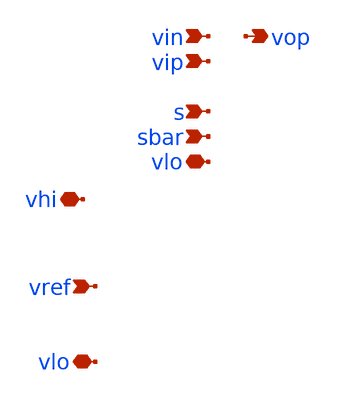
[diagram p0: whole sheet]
** sch_path: xschem/i_type_ota_gb_rp_gp_PEX.sch
**.subckt i_type_ota_gb_rp_gp_PEX vip vin vop vhi vlo vref s sbar vlo
*.ipin vip
*.ipin vin
*.opin vop
*.iopin vhi
*.iopin vlo
*.ipin vref
*.ipin s
*.ipin sbar
*.iopin vlo
**** begin user architecture code

* NGSPICE file created from cmota_1_flat.ext - technology: sky130A
* NGSPICE file created from cmota_gb_rp_gp.ext - technology: sky130A
.subckt imirror2 OUT a_5468_1540# a_4094_1540# a_4493_207# VLO VHI a_5868_1637# IN  a_4036_1637#
X0 VHI a_4493_207# a_4493_207# VHI.t5 sky130_fd_pr__pfet_01v8 ad=2.9e+12p pd=2.058e+07u as=2.9e+12p
+ ps=2.058e+07u w=1e+07u l=2e+06u
X1 a_4493_207# VLO.t6 VLO.t8 VLO.t7 sky130_fd_pr__nfet_01v8 ad=1.45e+12p pd=1.058e+07u as=0p ps=0u
+ w=5e+06u l=2e+06u
X2 VLO.t5 VLO.t3 OUT VLO.t4 sky130_fd_pr__nfet_01v8 ad=0p pd=0u as=1.45e+12p ps=1.058e+07u w=5e+06u
+ l=2e+06u
X3 a_5868_1637# a_5468_1540# OUT VHI.t0 sky130_fd_pr__pfet_01v8 ad=2.9e+12p pd=2.058e+07u
+ as=2.9e+12p ps=2.058e+07u w=1e+07u l=2e+06u
X4 OUT OUT.t0 VLO VLO.t0 sky130_fd_pr__nfet_01v8 ad=0p pd=0u as=4.35e+12p ps=3.174e+07u w=5e+06u
+ l=2e+06u
X5 VLO IN.t0 a_4493_207# VLO.t9 sky130_fd_pr__nfet_01v8 ad=0p pd=0u as=0p ps=0u w=5e+06u l=2e+06u
X6 a_4493_207# a_4094_1540# a_4036_1637# VHI.t1 sky130_fd_pr__pfet_01v8 ad=0p pd=0u as=2.9e+12p
+ ps=2.058e+07u w=1e+07u l=2e+06u
X7 OUT a_4493_207# VHI VHI.t2 sky130_fd_pr__pfet_01v8 ad=0p pd=0u as=0p ps=0u w=1e+07u l=2e+06u
R0 VHI.t2 VHI.t0 178.465
R1 VHI.t5 VHI.t1 178.465
R2 VHI.t0 VHI.n1 133.656
R3 VHI.t1 VHI.n3 133.656
R4 VHI.n6 VHI.t2 89.232
R5 VHI.n6 VHI.t5 89.232
R6 VHI.n9 VHI.n8 3.388
R7 VHI VHI.n9 1.702
R8 VHI.n5 VHI.n4 0.002
R9 VHI.n6 VHI.n5 0.002
R10 VHI.n8 VHI.n7 0.002
R11 VHI.n7 VHI.n6 0.002
R12 VHI.n3 VHI.n2 0.002
R13 VHI.n1 VHI.n0 0.002
R14 VLO.n4 VLO.t4 1062.83
R15 VLO.n7 VLO.t7 1062.83
R16 VLO.n15 VLO.t0 709.577
R17 VLO.n15 VLO.t9 709.577
R18 VLO.n13 VLO.n11 344.847
R19 VLO.n13 VLO.n12 344.847
R20 VLO.n6 VLO.n5 264.873
R21 VLO.n9 VLO.n8 264.496
R22 VLO.n21 VLO.n19 202.541
R23 VLO.n2 VLO.n0 202.541
R24 VLO.t6 VLO.n20 153.089
R25 VLO.n21 VLO.t6 153.089
R26 VLO.n2 VLO.t3 153.089
R27 VLO.t3 VLO.n1 153.089
R28 VLO.n22 VLO.n21 32.935
R29 VLO.n3 VLO.n2 32.935
R30 VLO.n24 VLO.n9 10.039
R31 VLO.n24 VLO.n6 10.037
R32 VLO.n24 VLO.n18 8.178
R33 VLO.n24 VLO.n23 8.178
R34 VLO.n23 VLO.n22 8.01
R35 VLO.n6 VLO.n3 6.032
R36 VLO.n24 VLO.n17 3.765
R37 VLO.n19 VLO.t8 3.48
R38 VLO.n0 VLO.t5 3.48
R39 VLO VLO.n24 1.562
R40 VLO.n17 VLO.n10 1.127
R41 VLO.n17 VLO.n16 0.014
R42 VLO.n16 VLO.n15 0.014
R43 VLO.n8 VLO.n7 0.012
R44 VLO.n5 VLO.n4 0.012
R45 VLO.n14 VLO.n13 0.007
R46 VLO.n15 VLO.n14 0.007
R47 OUT OUT.t0 68.216
R48 IN IN.t0 67.356
C0 a_4036_1637# VHI 0.68fF
C1 a_4493_207# VHI 3.25fF
C2 a_5468_1540# a_5868_1637# 0.15fF
C3 a_4094_1540# a_5868_1637# 0.01fF
C4 a_4493_207# a_4036_1637# 0.63fF
C5 IN OUT 0.22fF
C6 a_5468_1540# OUT 0.53fF
C7 a_4094_1540# OUT 0.10fF
C8 IN VHI 0.19fF
C9 a_5468_1540# VHI 0.99fF
C10 a_4036_1637# IN 0.03fF
C11 a_4094_1540# VHI 0.99fF
C12 a_4493_207# IN 0.46fF
C13 a_5468_1540# a_4036_1637# 0.01fF
C14 a_4493_207# a_5468_1540# 0.22fF
C15 a_4094_1540# a_4036_1637# 0.15fF
C16 a_4094_1540# a_4493_207# 0.44fF
C17 a_5868_1637# OUT 0.47fF
C18 a_5868_1637# VHI 0.45fF
C19 a_4493_207# a_5868_1637# 0.22fF
C20 a_4094_1540# IN 0.17fF
C21 a_4094_1540# a_5468_1540# 0.00fF
C22 VHI OUT 1.31fF
C23 a_4036_1637# OUT 0.03fF
C24 a_4493_207# OUT 0.88fF
C25 OUT VLO 5.14fF
C26 VHI VLO 19.08fF
C27 IN VLO 2.36fF
C28 a_5868_1637# VLO 0.34fF
C29 a_4036_1637# VLO 0.34fF
C30 a_5468_1540# VLO 0.34fF
C31 a_4493_207# VLO 1.55fF
C32 a_4094_1540# VLO 0.34fF
C33 OUT.t0 VLO 1.25fF
C34 VHI.n0 VLO 0.25fF $ **FLOATING
C35 VHI.n1 VLO 2.09fF $ **FLOATING
C36 VHI.t0 VLO 3.29fF
C37 VHI.t2 VLO 2.82fF
C38 VHI.n2 VLO 0.25fF $ **FLOATING
C39 VHI.n3 VLO 2.09fF $ **FLOATING
C40 VHI.t1 VLO 3.29fF
C41 VHI.t5 VLO 2.82fF
C42 VHI.n4 VLO 0.25fF $ **FLOATING
C43 VHI.n5 VLO 0.25fF $ **FLOATING
C44 VHI.n6 VLO 1.88fF $ **FLOATING
C45 VHI.n7 VLO 0.25fF $ **FLOATING
C46 VHI.n8 VLO 0.13fF $ **FLOATING
C47 VHI.n9 VLO 2.08fF $ **FLOATING
.ends

.subckt gated_iref_fix imirror2_0/a_5468_1540# imirror2_0/a_4094_1540# SBAR a_1444_106#
+  imirror2_0/OUT imirror2_0/a_5868_1637# VSUB imirror2_0/VHI imirror2_0/a_4493_207#  imirror2_0/a_4036_1637#
+ a_1712_150# S imirror2_0/IN
Ximirror2_0 imirror2_0/OUT imirror2_0/a_5468_1540# imirror2_0/a_4094_1540# imirror2_0/a_4493_207#
+  VSUB imirror2_0/VHI imirror2_0/a_5868_1637# imirror2_0/IN imirror2_0/a_4036_1637#  imirror2
X0 imirror2_0/OUT a_1444_106# VSUB sky130_fd_pr__res_xhigh_po w=350000u l=1.49e+06u
X1 VSUB SBAR a_1712_150# VSUB sky130_fd_pr__nfet_01v8 ad=5.95e+12p pd=4.302e+07u as=1.65e+12p
+ ps=1.132e+07u w=2.5e+06u l=150000u
X2 VSUB a_1712_150# sky130_fd_pr__cap_mim_m3_1 l=6.2e+06u w=2.76e+07u
X3 a_1712_150# VSUB sky130_fd_pr__cap_mim_m3_2 l=6.2e+06u w=2.76e+07u
X4 a_1712_150# S a_1444_106# VSUB sky130_fd_pr__nfet_01v8 ad=0p pd=0u as=1.6e+12p ps=1.128e+07u
+ w=2.5e+06u l=150000u
X5 VSUB VSUB a_1444_106# VSUB sky130_fd_pr__nfet_01v8 ad=0p pd=0u as=0p ps=0u w=2.5e+06u l=150000u
X6 a_1712_150# SBAR VSUB VSUB sky130_fd_pr__nfet_01v8 ad=0p pd=0u as=0p ps=0u w=2.5e+06u l=150000u
X7 a_1444_106# S a_1712_150# VSUB sky130_fd_pr__nfet_01v8 ad=0p pd=0u as=0p ps=0u w=2.5e+06u
+ l=150000u
C0 a_1712_150# imirror2_0/a_5868_1637# 0.33fF
C1 imirror2_0/OUT S 0.13fF
C2 imirror2_0/VHI imirror2_0/OUT 0.03fF
C3 imirror2_0/OUT imirror2_0/a_4493_207# 0.00fF
C4 a_1444_106# a_1712_150# 0.93fF
C5 SBAR a_1444_106# 0.07fF
C6 S a_1712_150# 0.27fF
C7 S SBAR 0.71fF
C8 imirror2_0/OUT a_1712_150# 1.57fF
C9 imirror2_0/VHI a_1712_150# 0.88fF
C10 imirror2_0/OUT SBAR 0.14fF
C11 a_1444_106# imirror2_0/IN 0.00fF
C12 S imirror2_0/IN 0.01fF
C13 a_1712_150# imirror2_0/a_4493_207# 0.29fF
C14 imirror2_0/OUT imirror2_0/IN 0.07fF
C15 imirror2_0/VHI imirror2_0/IN 0.00fF
C16 imirror2_0/OUT imirror2_0/a_5468_1540# 0.00fF
C17 SBAR a_1712_150# 0.25fF
C18 imirror2_0/a_4493_207# imirror2_0/IN 0.12fF
C19 a_1712_150# imirror2_0/IN 0.12fF
C20 SBAR imirror2_0/IN 0.01fF
C21 a_1712_150# imirror2_0/a_5468_1540# 0.33fF
C22 imirror2_0/OUT imirror2_0/a_5868_1637# 0.00fF
C23 S a_1444_106# 0.03fF
C24 imirror2_0/OUT a_1444_106# 0.33fF
C25 a_1712_150# VSUB 39.40fF
C26 a_1444_106# VSUB 1.29fF
C27 SBAR VSUB 0.76fF
C28 S VSUB 0.77fF
C29 imirror2_0/OUT VSUB 6.83fF
C30 imirror2_0/VHI VSUB 19.56fF
C31 imirror2_0/IN VSUB 4.59fF
C32 imirror2_0/a_5868_1637# VSUB 0.44fF
C33 imirror2_0/a_4036_1637# VSUB 0.34fF
C34 imirror2_0/a_5468_1540# VSUB 0.49fF
C35 imirror2_0/a_4493_207# VSUB 1.64fF
C36 imirror2_0/a_4094_1540# VSUB 0.34fF
C37 imirror2_0/OUT.t0 VSUB 1.25fF $ **FLOATING
C38 imirror2_0/VHI.n0 VSUB 0.25fF $ **FLOATING
C39 imirror2_0/VHI.n1 VSUB 2.09fF $ **FLOATING
C40 imirror2_0/VHI.t0 VSUB 3.29fF $ **FLOATING
C41 imirror2_0/VHI.t2 VSUB 2.82fF $ **FLOATING
C42 imirror2_0/VHI.n2 VSUB 0.25fF $ **FLOATING
C43 imirror2_0/VHI.n3 VSUB 2.09fF $ **FLOATING
C44 imirror2_0/VHI.t1 VSUB 3.29fF $ **FLOATING
C45 imirror2_0/VHI.t5 VSUB 2.82fF $ **FLOATING
C46 imirror2_0/VHI.n4 VSUB 0.25fF $ **FLOATING
C47 imirror2_0/VHI.n5 VSUB 0.25fF $ **FLOATING
C48 imirror2_0/VHI.n6 VSUB 1.88fF $ **FLOATING
C49 imirror2_0/VHI.n7 VSUB 0.25fF $ **FLOATING
C50 imirror2_0/VHI.n8 VSUB 0.13fF $ **FLOATING
C51 imirror2_0/VHI.n9 VSUB 2.08fF $ **FLOATING
.ends

.subckt sky130_fd_pr__res_high_po_0p69_G8QCSG a_48_n518# a_n186_n518# a_n316_n648#
X0 a_n186_n518# a_48_n518# a_n316_n648# sky130_fd_pr__res_high_po w=690000u l=5.83e+06u
C0 a_n186_n518# a_48_n518# 0.18fF
C1 a_48_n518# a_n316_n648# 0.52fF
C2 a_n186_n518# a_n316_n648# 0.52fF
.ends

.subckt cmota_gb_rp VREF COM VIP VIN DP li_5300_n960# VLO a_2217_285# DN VOP VMN VHI  a_2925_285#
Xsky130_fd_pr__res_high_po_0p69_G8QCSG_0 li_5300_n960# VMN VLO sky130_fd_pr__res_high_po_0p69_G8QCSG
X0 VHI DN VMN VHI sky130_fd_pr__pfet_01v8 ad=4.93e+13p pd=3.4986e+08u as=1.16e+13p ps=8.232e+07u
+ w=1e+07u l=300000u
X1 VHI DN DN VHI sky130_fd_pr__pfet_01v8 ad=0p pd=0u as=8.7e+12p ps=6.174e+07u w=1e+07u l=300000u
X2 VHI DP VOP VHI sky130_fd_pr__pfet_01v8 ad=0p pd=0u as=1.16e+13p ps=8.232e+07u w=1e+07u l=300000u
X3 DN VIN COM VLO sky130_fd_pr__nfet_01v8_lvt ad=3.3e+12p pd=2.264e+07u as=1.3225e+13p ps=9.21e+07u
+ w=2.5e+06u l=150000u
X4 COM VIN DN VLO sky130_fd_pr__nfet_01v8_lvt ad=0p pd=0u as=0p ps=0u w=2.5e+06u l=150000u
X5 DP VIP COM VLO sky130_fd_pr__nfet_01v8_lvt ad=3.3e+12p pd=2.264e+07u as=0p ps=0u w=2.5e+06u
+ l=150000u
X6 VMN DN VHI VHI sky130_fd_pr__pfet_01v8 ad=0p pd=0u as=0p ps=0u w=1e+07u l=300000u
X7 VMN DN VHI VHI sky130_fd_pr__pfet_01v8 ad=0p pd=0u as=0p ps=0u w=1e+07u l=300000u
X8 VHI VHI VOP VHI sky130_fd_pr__pfet_01v8 ad=0p pd=0u as=0p ps=0u w=1e+07u l=300000u
X9 a_2925_285# DN VHI VHI sky130_fd_pr__pfet_01v8 ad=2.9e+12p pd=2.058e+07u as=0p ps=0u w=1e+07u
+ l=300000u
X10 DP VIP COM VLO sky130_fd_pr__nfet_01v8_lvt ad=0p pd=0u as=0p ps=0u w=2.5e+06u l=150000u
X11 li_5300_n960# VOP sky130_fd_pr__cap_mim_m3_2 l=1.32e+07u w=3.7e+06u
X12 VOP DP VHI VHI sky130_fd_pr__pfet_01v8 ad=0p pd=0u as=0p ps=0u w=1e+07u l=300000u
X13 VOP DP VHI VHI sky130_fd_pr__pfet_01v8 ad=0p pd=0u as=0p ps=0u w=1e+07u l=300000u
X14 VOP DP VHI VHI sky130_fd_pr__pfet_01v8 ad=0p pd=0u as=0p ps=0u w=1e+07u l=300000u
X15 COM VLO VLO VLO sky130_fd_pr__nfet_01v8_lvt ad=0p pd=0u as=3.8e+13p ps=2.69525e+08u w=2.5e+06u
+ l=150000u
X16 VLO VMN VOP VLO sky130_fd_pr__nfet_01v8 ad=0p pd=0u as=5.8e+12p ps=4.116e+07u w=1e+07u l=300000u
X17 VHI DN VMN VHI sky130_fd_pr__pfet_01v8 ad=0p pd=0u as=0p ps=0u w=1e+07u l=300000u
X18 VLO VLO VLO VLO sky130_fd_pr__nfet_01v8 ad=0p pd=0u as=0p ps=0u w=1e+07u l=300000u
X19 VHI DN DP VHI sky130_fd_pr__pfet_01v8 ad=0p pd=0u as=8.7e+12p ps=6.174e+07u w=1e+07u l=300000u
X20 VHI DP DP VHI sky130_fd_pr__pfet_01v8 ad=0p pd=0u as=0p ps=0u w=1e+07u l=300000u
X21 COM VIP DP VLO sky130_fd_pr__nfet_01v8_lvt ad=0p pd=0u as=0p ps=0u w=2.5e+06u l=150000u
X22 VLO VREF COM VLO sky130_fd_pr__nfet_01v8 ad=0p pd=0u as=0p ps=0u w=1e+07u l=2e+06u
X23 VMN VHI VHI VHI sky130_fd_pr__pfet_01v8 ad=0p pd=0u as=0p ps=0u w=1e+07u l=300000u
X24 DN DN VHI VHI sky130_fd_pr__pfet_01v8 ad=0p pd=0u as=0p ps=0u w=1e+07u l=300000u
X25 VHI DP VOP VHI sky130_fd_pr__pfet_01v8 ad=0p pd=0u as=0p ps=0u w=1e+07u l=300000u
X26 VLO VLO VLO VLO sky130_fd_pr__nfet_01v8_lvt ad=0p pd=0u as=0p ps=0u w=2.5e+06u l=150000u
X27 VLO VREF COM VLO sky130_fd_pr__nfet_01v8 ad=0p pd=0u as=0p ps=0u w=1e+07u l=2e+06u
X28 COM VIN DN VLO sky130_fd_pr__nfet_01v8_lvt ad=0p pd=0u as=0p ps=0u w=2.5e+06u l=150000u
X29 DN DN VHI VHI sky130_fd_pr__pfet_01v8 ad=0p pd=0u as=0p ps=0u w=1e+07u l=300000u
X30 DP DN VHI VHI sky130_fd_pr__pfet_01v8 ad=0p pd=0u as=0p ps=0u w=1e+07u l=300000u
X31 DN DP VHI VHI sky130_fd_pr__pfet_01v8 ad=0p pd=0u as=0p ps=0u w=1e+07u l=300000u
X32 DP DP VHI VHI sky130_fd_pr__pfet_01v8 ad=0p pd=0u as=0p ps=0u w=1e+07u l=300000u
X33 DN VIN COM VLO sky130_fd_pr__nfet_01v8_lvt ad=0p pd=0u as=0p ps=0u w=2.5e+06u l=150000u
X34 VLO VLO VLO VLO sky130_fd_pr__nfet_01v8 ad=0p pd=0u as=0p ps=0u w=1e+07u l=300000u
X35 COM VIP DP VLO sky130_fd_pr__nfet_01v8_lvt ad=0p pd=0u as=0p ps=0u w=2.5e+06u l=150000u
X36 VHI DN DN VHI sky130_fd_pr__pfet_01v8 ad=0p pd=0u as=0p ps=0u w=1e+07u l=300000u
X37 VOP DP VHI VHI sky130_fd_pr__pfet_01v8 ad=0p pd=0u as=0p ps=0u w=1e+07u l=300000u
X38 VMN VMN VLO VLO sky130_fd_pr__nfet_01v8 ad=5.8e+12p pd=4.116e+07u as=0p ps=0u w=1e+07u l=300000u
X39 VLO VMN VMN VLO sky130_fd_pr__nfet_01v8 ad=0p pd=0u as=0p ps=0u w=1e+07u l=300000u
X40 VLO VLO VLO VLO sky130_fd_pr__nfet_01v8 ad=0p pd=0u as=0p ps=0u w=1e+07u l=300000u
X41 VOP VMN VLO VLO sky130_fd_pr__nfet_01v8 ad=0p pd=0u as=0p ps=0u w=1e+07u l=300000u
X42 VHI DP DN VHI sky130_fd_pr__pfet_01v8 ad=0p pd=0u as=0p ps=0u w=1e+07u l=300000u
X43 VLO VMN VOP VLO sky130_fd_pr__nfet_01v8 ad=0p pd=0u as=0p ps=0u w=1e+07u l=300000u
X44 VHI DN VMN VHI sky130_fd_pr__pfet_01v8 ad=0p pd=0u as=0p ps=0u w=1e+07u l=300000u
X45 VLO VLO COM VLO sky130_fd_pr__nfet_01v8_lvt ad=0p pd=0u as=0p ps=0u w=2.5e+06u l=150000u
X46 DN VIN COM VLO sky130_fd_pr__nfet_01v8_lvt ad=0p pd=0u as=0p ps=0u w=2.5e+06u l=150000u
X47 VHI DP a_2217_285# VHI sky130_fd_pr__pfet_01v8 ad=0p pd=0u as=2.9e+12p ps=2.058e+07u w=1e+07u
+ l=300000u
X48 VHI DP DP VHI sky130_fd_pr__pfet_01v8 ad=0p pd=0u as=0p ps=0u w=1e+07u l=300000u
X49 VLO VLO VLO VLO sky130_fd_pr__nfet_01v8 ad=0p pd=0u as=0p ps=0u w=1e+07u l=300000u
X50 COM VREF VLO VLO sky130_fd_pr__nfet_01v8 ad=0p pd=0u as=0p ps=0u w=1e+07u l=2e+06u
X51 VLO VLO VLO VLO sky130_fd_pr__nfet_01v8_lvt ad=0p pd=0u as=0p ps=0u w=2.5e+06u l=150000u
X52 COM VIN DN VLO sky130_fd_pr__nfet_01v8_lvt ad=0p pd=0u as=0p ps=0u w=2.5e+06u l=150000u
X53 COM VREF VLO VLO sky130_fd_pr__nfet_01v8 ad=0p pd=0u as=0p ps=0u w=1e+07u l=2e+06u
X54 DP VIP COM VLO sky130_fd_pr__nfet_01v8_lvt ad=0p pd=0u as=0p ps=0u w=2.5e+06u l=150000u
X55 COM VIN DN VLO sky130_fd_pr__nfet_01v8_lvt ad=0p pd=0u as=0p ps=0u w=2.5e+06u l=150000u
X56 VMN DN VHI VHI sky130_fd_pr__pfet_01v8 ad=0p pd=0u as=0p ps=0u w=1e+07u l=300000u
X57 DP DP VHI VHI sky130_fd_pr__pfet_01v8 ad=0p pd=0u as=0p ps=0u w=1e+07u l=300000u
X58 DP VIP COM VLO sky130_fd_pr__nfet_01v8_lvt ad=0p pd=0u as=0p ps=0u w=2.5e+06u l=150000u
X59 a_2217_285# DP VHI VHI sky130_fd_pr__pfet_01v8 ad=0p pd=0u as=0p ps=0u w=1e+07u l=300000u
X60 VMN VMN VLO VLO sky130_fd_pr__nfet_01v8 ad=0p pd=0u as=0p ps=0u w=1e+07u l=300000u
X61 COM VIP DP VLO sky130_fd_pr__nfet_01v8_lvt ad=0p pd=0u as=0p ps=0u w=2.5e+06u l=150000u
X62 VLO VMN VMN VLO sky130_fd_pr__nfet_01v8 ad=0p pd=0u as=0p ps=0u w=1e+07u l=300000u
X63 VOP VMN VLO VLO sky130_fd_pr__nfet_01v8 ad=0p pd=0u as=0p ps=0u w=1e+07u l=300000u
X64 COM VIP DP VLO sky130_fd_pr__nfet_01v8_lvt ad=0p pd=0u as=0p ps=0u w=2.5e+06u l=150000u
X65 VHI DN VMN VHI sky130_fd_pr__pfet_01v8 ad=0p pd=0u as=0p ps=0u w=1e+07u l=300000u
X66 DN VIN COM VLO sky130_fd_pr__nfet_01v8_lvt ad=0p pd=0u as=0p ps=0u w=2.5e+06u l=150000u
X67 VOP li_5300_n960# sky130_fd_pr__cap_mim_m3_1 l=1.32e+07u w=3.7e+06u
X68 VHI DN a_2925_285# VHI sky130_fd_pr__pfet_01v8 ad=0p pd=0u as=0p ps=0u w=1e+07u l=300000u
X69 VHI DP VOP VHI sky130_fd_pr__pfet_01v8 ad=0p pd=0u as=0p ps=0u w=1e+07u l=300000u
C0 VOP VREF 0.03fF
C1 DN COM 6.05fF
C2 VOP VIP 0.01fF
C3 VMN VREF 0.10fF
C4 li_5300_n960# DP 0.48fF
C5 VOP a_2217_285# 0.01fF
C6 VMN VIP 0.14fF
C7 VHI a_2925_285# 4.31fF
C8 DN DP 1.21fF
C9 VHI VIN 0.11fF
C10 VMN a_2217_285# 0.06fF
C11 COM a_2925_285# 0.01fF
C12 VIN COM 0.71fF
C13 VHI VREF 0.04fF
C14 COM VREF 2.35fF
C15 VHI VIP 0.10fF
C16 DP a_2925_285# 0.17fF
C17 VHI a_2217_285# 4.31fF
C18 COM VIP 0.71fF
C19 VIN DP 0.04fF
C20 a_2217_285# COM 0.01fF
C21 DP VREF 0.14fF
C22 VIP DP 0.53fF
C23 a_2217_285# DP 0.13fF
C24 DN a_2925_285# 0.13fF
C25 DN VIN 0.53fF
C26 DN VREF 0.14fF
C27 DN VIP 0.05fF
C28 VMN VOP 0.72fF
C29 DN a_2217_285# 0.17fF
C30 VREF a_2925_285# 0.00fF
C31 VIN VREF 0.36fF
C32 VIP a_2925_285# 0.00fF
C33 VIN VIP 0.11fF
C34 VHI VOP 18.23fF
C35 a_2217_285# a_2925_285# 0.02fF
C36 a_2217_285# VIN 0.00fF
C37 VOP COM 0.05fF
C38 VIP VREF 0.36fF
C39 VHI VMN 17.75fF
C40 a_2217_285# VREF 0.00fF
C41 VMN COM 0.33fF
C42 VOP DP 0.97fF
C43 VMN DP 0.34fF
C44 VHI COM 0.10fF
C45 li_5300_n960# VOP 9.33fF
C46 VHI DP 16.22fF
C47 VMN li_5300_n960# 1.12fF
C48 DN VOP 0.06fF
C49 COM DP 6.02fF
C50 DN VMN 1.12fF
C51 VHI li_5300_n960# 2.02fF
C52 VOP a_2925_285# 0.05fF
C53 VHI DN 16.22fF
C54 VMN a_2925_285# 0.01fF
C55 VMN VIN 0.15fF
C56 VREF VLO 7.20fF
C57 COM VLO 6.11fF
C58 VIP VLO 0.78fF
C59 VIN VLO 0.79fF
C60 VOP VLO 9.34fF
C61 a_2925_285# VLO -0.04fF
C62 a_2217_285# VLO -0.04fF
C63 DP VLO 1.36fF
C64 DN VLO 1.42fF
C65 VHI VLO 35.14fF
C66 li_5300_n960# VLO 3.02fF
C67 VMN VLO 13.45fF
.ends

.subckt cmota_gb_rp_gp VHI VLO VREF VIP VIN VOP S SBAR
Xgated_iref_fix_0 gated_iref_fix_0/imirror2_0/a_5468_1540# gated_iref_fix_0/imirror2_0/a_4094_1540#
+  SBAR gated_iref_fix_0/a_1444_106# gated_iref_fix_0/imirror2_0/OUT
+ gated_iref_fix_0/imirror2_0/a_5868_1637#  VLO VHI gated_iref_fix_0/imirror2_0/a_4493_207# gated_iref_fix_0/imirror2_0/a_4036_1637#
+  VREF_GATED S VREF gated_iref_fix
Xcmota_gb_rp_0 VREF_GATED cmota_gb_rp_0/COM VIP VIN cmota_gb_rp_0/DP cmota_gb_rp_0/li_5300_n960#
+  VLO cmota_gb_rp_0/a_2217_285# cmota_gb_rp_0/DN VOP cmota_gb_rp_0/VMN VHI cmota_gb_rp_0/a_2925_285#
+  cmota_gb_rp
X0 VLO VHI sky130_fd_pr__cap_mim_m3_2 l=3.1e+07u w=1.3e+07u
X1 VHI VLO sky130_fd_pr__cap_mim_m3_1 l=3.1e+07u w=1.3e+07u
C0 cmota_gb_rp_0/VMN VIN -0.00fF
C1 VREF_GATED cmota_gb_rp_0/VMN 1.54fF
C2 cmota_gb_rp_0/DN VHI 0.89fF
C3 VIN VIP 0.00fF
C4 VREF gated_iref_fix_0/a_1444_106# 0.00fF
C5 VREF S 0.03fF
C6 VREF gated_iref_fix_0/imirror2_0/OUT 0.00fF
C7 VREF_GATED VREF -0.04fF
C8 gated_iref_fix_0/imirror2_0/a_5868_1637# VHI 0.03fF
C9 VOP cmota_gb_rp_0/VMN 0.00fF
C10 VHI gated_iref_fix_0/a_1444_106# 0.00fF
C11 VREF_GATED gated_iref_fix_0/imirror2_0/a_5468_1540# -0.31fF
C12 cmota_gb_rp_0/a_2925_285# VHI 0.04fF
C13 VHI S 0.00fF
C14 cmota_gb_rp_0/DP VHI 0.81fF
C15 VIN cmota_gb_rp_0/COM -0.00fF
C16 VHI gated_iref_fix_0/imirror2_0/OUT 0.17fF
C17 VREF_GATED cmota_gb_rp_0/COM 0.17fF
C18 VREF_GATED cmota_gb_rp_0/DN 0.40fF
C19 VREF_GATED VHI 3.68fF
C20 VREF SBAR 0.02fF
C21 VOP cmota_gb_rp_0/li_5300_n960# 0.00fF
C22 VREF_GATED gated_iref_fix_0/imirror2_0/a_5868_1637# -0.07fF
C23 gated_iref_fix_0/imirror2_0/a_4036_1637# VHI 0.07fF
C24 VREF_GATED gated_iref_fix_0/a_1444_106# 0.00fF
C25 VOP VHI 0.11fF
C26 gated_iref_fix_0/imirror2_0/a_4493_207# VHI 0.19fF
C27 gated_iref_fix_0/imirror2_0/OUT S 0.00fF
C28 VHI SBAR 0.00fF
C29 cmota_gb_rp_0/VMN cmota_gb_rp_0/COM -0.00fF
C30 VREF_GATED S 0.00fF
C31 VHI cmota_gb_rp_0/VMN 0.15fF
C32 VREF_GATED gated_iref_fix_0/imirror2_0/OUT -0.37fF
C33 VREF_GATED VIN 0.00fF
C34 SBAR gated_iref_fix_0/a_1444_106# 0.00fF
C35 VREF VHI 0.16fF
C36 S SBAR 0.10fF
C37 cmota_gb_rp_0/DP VOP -0.00fF
C38 gated_iref_fix_0/imirror2_0/a_5468_1540# VHI 0.00fF
C39 gated_iref_fix_0/imirror2_0/OUT SBAR 0.00fF
C40 VHI cmota_gb_rp_0/li_5300_n960# 0.03fF
C41 VREF_GATED gated_iref_fix_0/imirror2_0/a_4493_207# -0.29fF
C42 VREF_GATED SBAR 0.02fF
C43 cmota_gb_rp_0/a_2217_285# VHI 0.04fF
C44 gated_iref_fix_0/imirror2_0/a_4094_1540# VHI 0.01fF
C45 VREF_GATED VLO 52.16fF
C46 cmota_gb_rp_0/COM VLO 6.15fF
C47 VIP VLO 0.78fF
C48 VIN VLO 0.79fF
C49 VOP VLO 9.31fF
C50 cmota_gb_rp_0/a_2925_285# VLO -0.04fF
C51 cmota_gb_rp_0/a_2217_285# VLO -0.04fF
C52 cmota_gb_rp_0/DP VLO 1.36fF
C53 cmota_gb_rp_0/DN VLO 1.55fF
C54 cmota_gb_rp_0/li_5300_n960# VLO 2.88fF
C55 cmota_gb_rp_0/VMN VLO 14.06fF
C56 gated_iref_fix_0/a_1444_106# VLO 1.29fF
C57 SBAR VLO 0.76fF
C58 S VLO 0.78fF
C59 gated_iref_fix_0/imirror2_0/OUT VLO 8.38fF
C60 VHI VLO 134.49fF
C61 VREF VLO 6.75fF
C62 gated_iref_fix_0/imirror2_0/a_5868_1637# VLO 0.48fF
C63 gated_iref_fix_0/imirror2_0/a_4036_1637# VLO 0.88fF
C64 gated_iref_fix_0/imirror2_0/a_5468_1540# VLO 0.63fF
C65 gated_iref_fix_0/imirror2_0/a_4493_207# VLO 4.55fF
C66 gated_iref_fix_0/imirror2_0/a_4094_1540# VLO 0.94fF
C67 gated_iref_fix_0/imirror2_0/OUT.t0 VLO 1.25fF $ **FLOATING
C68 gated_iref_fix_0/imirror2_0/VHI.n0 VLO 0.25fF $ **FLOATING
C69 gated_iref_fix_0/imirror2_0/VHI.n1 VLO 2.09fF $ **FLOATING
C70 gated_iref_fix_0/imirror2_0/VHI.t0 VLO 3.29fF $ **FLOATING
C71 gated_iref_fix_0/imirror2_0/VHI.t2 VLO 2.82fF $ **FLOATING
C72 gated_iref_fix_0/imirror2_0/VHI.n2 VLO 0.25fF $ **FLOATING
C73 gated_iref_fix_0/imirror2_0/VHI.n3 VLO 2.09fF $ **FLOATING
C74 gated_iref_fix_0/imirror2_0/VHI.t1 VLO 3.29fF $ **FLOATING
C75 gated_iref_fix_0/imirror2_0/VHI.t5 VLO 2.82fF $ **FLOATING
C76 gated_iref_fix_0/imirror2_0/VHI.n4 VLO 0.25fF $ **FLOATING
C77 gated_iref_fix_0/imirror2_0/VHI.n5 VLO 0.25fF $ **FLOATING
C78 gated_iref_fix_0/imirror2_0/VHI.n6 VLO 1.88fF $ **FLOATING
C79 gated_iref_fix_0/imirror2_0/VHI.n7 VLO 0.25fF $ **FLOATING
C80 gated_iref_fix_0/imirror2_0/VHI.n8 VLO 0.13fF $ **FLOATING
C81 gated_iref_fix_0/imirror2_0/VHI.n9 VLO 2.08fF $ **FLOATING
.ends



XDUT vhi vlo vref vip vin vop s sbar cmota_gb_rp_gp


**** end user architecture code
**.ends
.end
